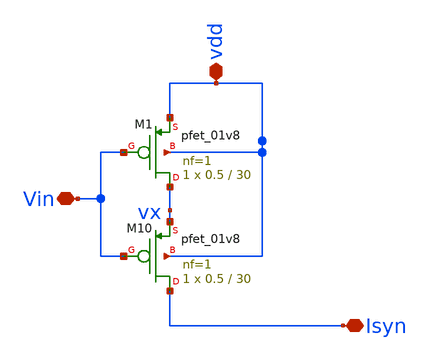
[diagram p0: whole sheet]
** sch_path: Neuron/ultralif/syn_neg.sch
**.subckt syn_neg Vin Isyn vdd
*.iopin Vin
*.iopin Isyn
*.iopin vdd
XM10 Isyn Vin vx vdd sky130_fd_pr__pfet_01v8 L=30 W=0.5 nf=1 ad='int((nf+1)/2) * W/nf * 0.29' as='int((nf+2)/2) * W/nf * 0.29'
+ pd='2*int((nf+1)/2) * (W/nf + 0.29)' ps='2*int((nf+2)/2) * (W/nf + 0.29)' nrd='0.29 / W' nrs='0.29 / W'
+ sa=0 sb=0 sd=0 mult=1 m=1
XM1 vx Vin vdd vdd sky130_fd_pr__pfet_01v8 L=30 W=0.5 nf=1 ad='int((nf+1)/2) * W/nf * 0.29' as='int((nf+2)/2) * W/nf * 0.29'
+ pd='2*int((nf+1)/2) * (W/nf + 0.29)' ps='2*int((nf+2)/2) * (W/nf + 0.29)' nrd='0.29 / W' nrs='0.29 / W'
+ sa=0 sb=0 sd=0 mult=1 m=1
**.ends
.end
